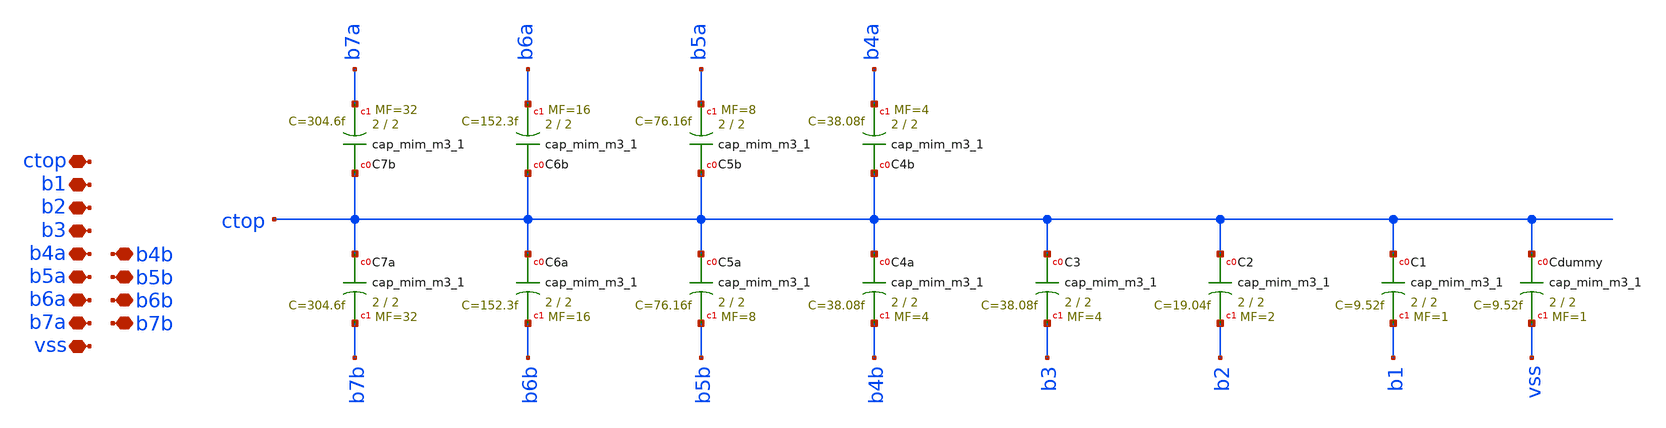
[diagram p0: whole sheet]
** sch_path: xschem/sar-adc/cdac.sch
**.subckt cdac ctop b1 b2 b3 b4a b5a b6a b7a b5b b4b b6b b7b vss
*.iopin ctop
*.iopin b1
*.iopin b2
*.iopin b3
*.iopin b4a
*.iopin b5a
*.iopin b6a
*.iopin b7a
*.iopin b5b
*.iopin b4b
*.iopin b6b
*.iopin b7b
*.iopin vss
XC1 ctop b1 sky130_fd_pr__cap_mim_m3_1 W=2 L=2 MF=1 m=1
XC2 ctop b2 sky130_fd_pr__cap_mim_m3_1 W=2 L=2 MF=2 m=2
XC3 ctop b3 sky130_fd_pr__cap_mim_m3_1 W=2 L=2 MF=4 m=4
XC4a ctop b4b sky130_fd_pr__cap_mim_m3_1 W=2 L=2 MF=4 m=4
XC5a ctop b5b sky130_fd_pr__cap_mim_m3_1 W=2 L=2 MF=8 m=8
XC6a ctop b6b sky130_fd_pr__cap_mim_m3_1 W=2 L=2 MF=16 m=16
XC7a ctop b7b sky130_fd_pr__cap_mim_m3_1 W=2 L=2 MF=32 m=32
XCdummy ctop vss sky130_fd_pr__cap_mim_m3_1 W=2 L=2 MF=1 m=1
XC7b ctop b7a sky130_fd_pr__cap_mim_m3_1 W=2 L=2 MF=32 m=32
XC6b ctop b6a sky130_fd_pr__cap_mim_m3_1 W=2 L=2 MF=16 m=16
XC5b ctop b5a sky130_fd_pr__cap_mim_m3_1 W=2 L=2 MF=8 m=8
XC4b ctop b4a sky130_fd_pr__cap_mim_m3_1 W=2 L=2 MF=4 m=4
**.ends
.end
